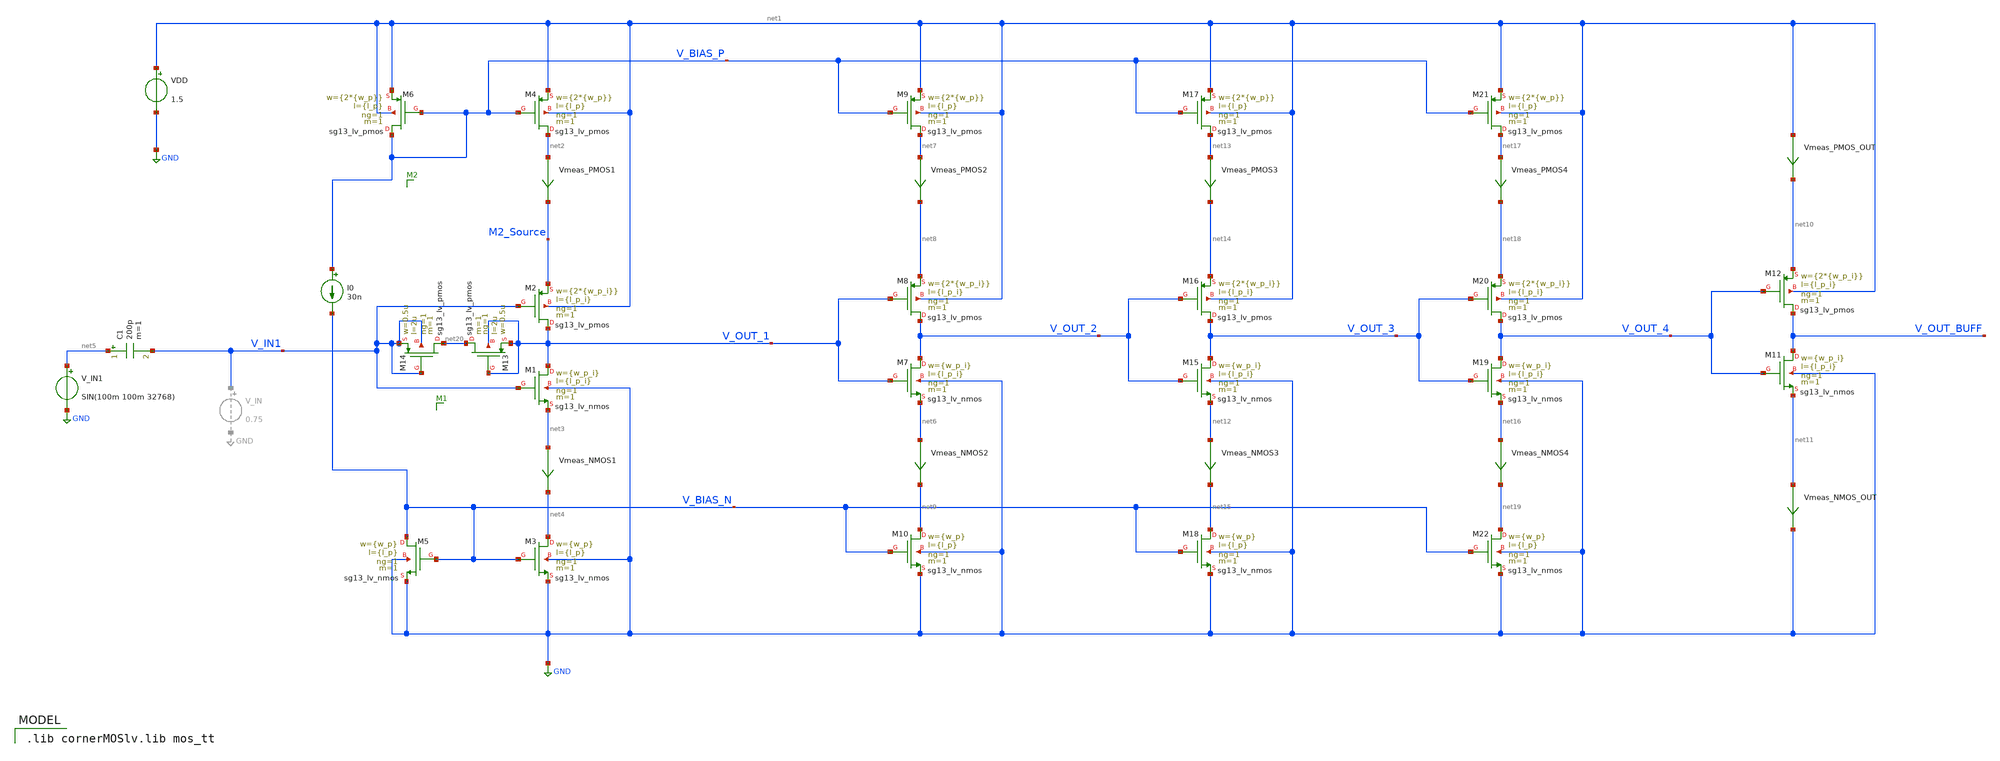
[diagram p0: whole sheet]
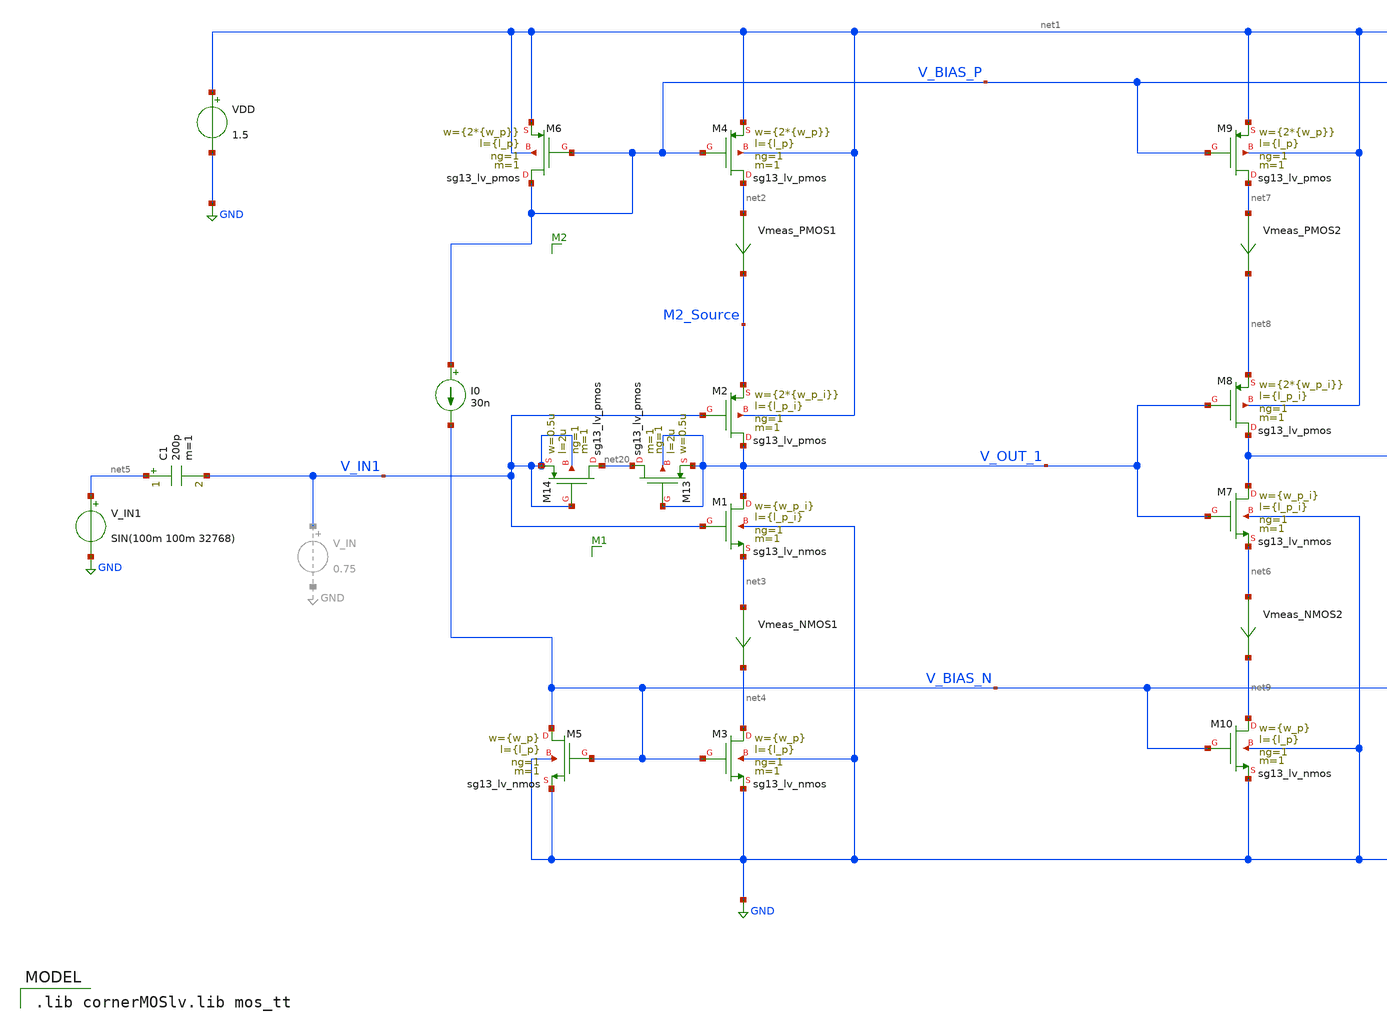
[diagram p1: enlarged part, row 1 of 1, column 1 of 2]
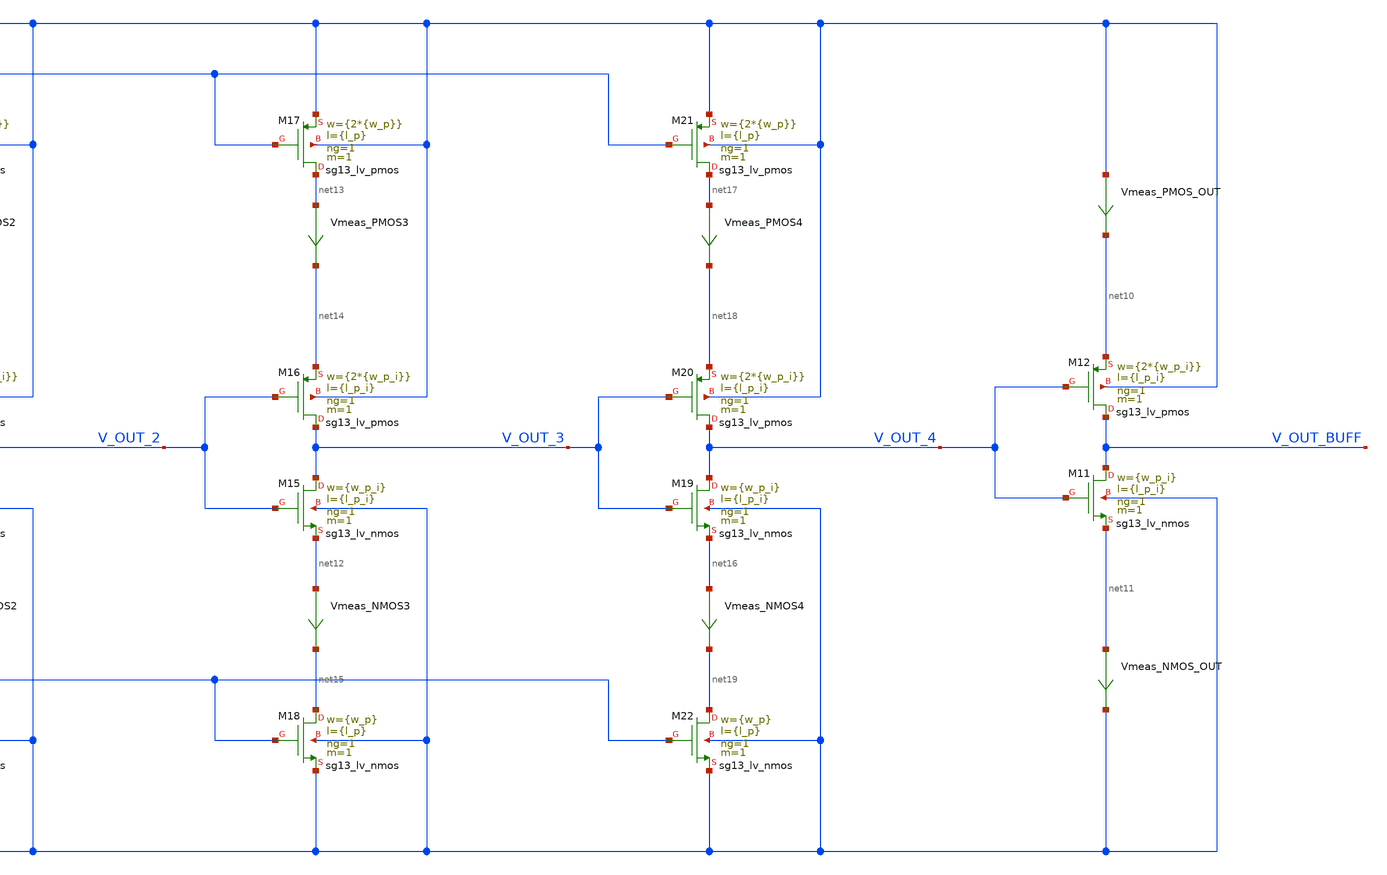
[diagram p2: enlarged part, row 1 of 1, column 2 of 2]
** sch_path: inverter_starved_v1_playground.sch
**.subckt inverter_starved_v1_playground
XM1 V_OUT_1 V_IN1 net3 GND sg13_lv_nmos w={w_p_i} l={l_p_i} ng=1 m=1 mm_ok=1
XM2 V_OUT_1 V_IN1 M2_Source net1 sg13_lv_pmos w={2*{w_p_i}} l={l_p_i} ng=1 m=1 mm_ok=1
VDD net1 GND 1.5
XM3 net4 V_BIAS_N GND GND sg13_lv_nmos w={w_p} l={l_p} ng=1 m=1 mm_ok=1
XM4 net2 V_BIAS_P net1 net1 sg13_lv_pmos w={2*{w_p}} l={l_p} ng=1 m=1 mm_ok=1
XM5 V_BIAS_N V_BIAS_N GND GND sg13_lv_nmos w={w_p} l={l_p} ng=1 m=1 mm_ok=1
XM6 V_BIAS_P V_BIAS_P net1 net1 sg13_lv_pmos w={2*{w_p}} l={l_p} ng=1 m=1 mm_ok=1
I0 V_BIAS_P V_BIAS_N 30n
Vmeas_PMOS1 net2 M2_Source 0
.save i(vmeas_pmos1)
Vmeas_NMOS1 net3 net4 0
.save i(vmeas_nmos1)
V_IN1 net5 GND SIN(100m 100m 32768)
C1 net5 V_IN1 200p m=1
XM7 V_OUT_2 V_OUT_1 net6 GND sg13_lv_nmos w={w_p_i} l={l_p_i} ng=1 m=1 mm_ok=1
XM8 V_OUT_2 V_OUT_1 net8 net1 sg13_lv_pmos w={2*{w_p_i}} l={l_p_i} ng=1 m=1 mm_ok=1
Vmeas_NMOS2 net6 net9 0
.save i(vmeas_nmos2)
XM9 net7 V_BIAS_P net1 net1 sg13_lv_pmos w={2*{w_p}} l={l_p} ng=1 m=1 mm_ok=1
Vmeas_PMOS2 net7 net8 0
.save i(vmeas_pmos2)
XM10 net9 V_BIAS_N GND GND sg13_lv_nmos w={w_p} l={l_p} ng=1 m=1 mm_ok=1
XM11 V_OUT_BUFF V_OUT_4 net11 GND sg13_lv_nmos w={w_p_i} l={l_p_i} ng=1 m=1 mm_ok=1
XM12 V_OUT_BUFF V_OUT_4 net10 net1 sg13_lv_pmos w={2*{w_p_i}} l={l_p_i} ng=1 m=1 mm_ok=1
XM13 net20 V_OUT_1 V_OUT_1 V_OUT_1 sg13_lv_pmos w=0.5u l=2u ng=1 m=1 mm_ok=1
XM14 net20 V_IN1 V_IN1 V_IN1 sg13_lv_pmos w=0.5u l=2u ng=1 m=1 mm_ok=1
Vmeas_PMOS_OUT net1 net10 0
.save i(vmeas_pmos_out)
Vmeas_NMOS_OUT net11 GND 0
.save i(vmeas_nmos_out)
XM15 V_OUT_3 V_OUT_2 net12 GND sg13_lv_nmos w={w_p_i} l={l_p_i} ng=1 m=1 mm_ok=1
XM16 V_OUT_3 V_OUT_2 net14 net1 sg13_lv_pmos w={2*{w_p_i}} l={l_p_i} ng=1 m=1 mm_ok=1
Vmeas_NMOS3 net12 net15 0
.save i(vmeas_nmos3)
XM17 net13 V_BIAS_P net1 net1 sg13_lv_pmos w={2*{w_p}} l={l_p} ng=1 m=1 mm_ok=1
Vmeas_PMOS3 net13 net14 0
.save i(vmeas_pmos3)
XM18 net15 V_BIAS_N GND GND sg13_lv_nmos w={w_p} l={l_p} ng=1 m=1 mm_ok=1
XM19 V_OUT_4 V_OUT_3 net16 GND sg13_lv_nmos w={w_p_i} l={l_p_i} ng=1 m=1 mm_ok=1
XM20 V_OUT_4 V_OUT_3 net18 net1 sg13_lv_pmos w={2*{w_p_i}} l={l_p_i} ng=1 m=1 mm_ok=1
Vmeas_NMOS4 net16 net19 0
.save i(vmeas_nmos4)
XM21 net17 V_BIAS_P net1 net1 sg13_lv_pmos w={2*{w_p}} l={l_p} ng=1 m=1 mm_ok=1
Vmeas_PMOS4 net17 net18 0
.save i(vmeas_pmos4)
XM22 net19 V_BIAS_N GND GND sg13_lv_nmos w={w_p} l={l_p} ng=1 m=1 mm_ok=1
**** begin user architecture code
 .lib cornerMOSlv.lib mos_tt



.include inverter_starved_playground.save
.param w_p_i=0.4u l_p_i=0.13u
*.param w_p_i=0.65u l_p_i=0.145u
.param w_p=0.4u l_p=0.13u
.meas tran iavg_stage_1_pmos AVG i(Vmeas_PMOS1)
.meas tran iavg_stage_1_nmos AVG i(Vmeas_NMOS1)
.meas tran iavg_stage_2_pmos AVG i(Vmeas_PMOS2)
.meas tran iavg_stage_2_nmos AVG i(Vmeas_NMOS2)
.meas tran iavg_stage_3_pmos AVG i(Vmeas_PMOS3)
.meas tran iavg_stage_3_nmos AVG i(Vmeas_NMOS3)
.meas tran iavg_stage_4_pmos AVG i(Vmeas_PMOS4)
.meas tran iavg_stage_4_nmos AVG i(Vmeas_NMOS4)
.meas tran iavg_stage_5_pmos AVG i(Vmeas_PMOS_OUT)
.meas tran iavg_stage_5_nmos AVG i(Vmeas_NMOS_OUT)
.meas tran iavg_VDD AVG i(VDD)

.control
*save all
save V_OUT_BUFF

op
write inverter_starved_v1_playground.raw
set appendwrite

tran 0.05u 2m

*plot V_IN1 V_OUT_1 V_OUT_2 V_OUT_3 V_OUT_4 V_OUT_BUFF
*plot V_IN1 V_OUT_1 V_OUT_BUFF


*linearize V_OUT_BUFF
*fft V_OUT_BUFF
*plot mag(V_OUT_BUFF)

*.measure tran yrms RMS i(VDD) from=0.1m to=0.2m

.endc


**** end user architecture code
**.ends
.GLOBAL GND
.end
